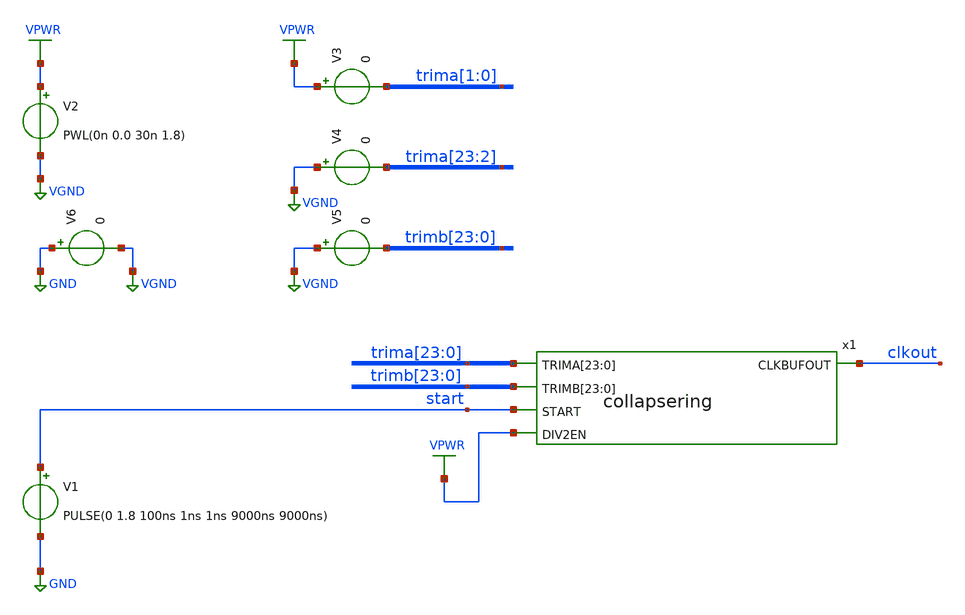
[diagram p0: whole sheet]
** sch_path: ip/randsack/sch/collapsering_tb.sch
**.subckt collapsering_tb
V1 start GND PULSE(0 1.8 100ns 1ns 1ns 9000ns 9000ns)
V2 VPWR VGND PWL(0n 0.0 30n 1.8)
x1 trima[23] trima[22] trima[21] trima[20] trima[19] trima[18] trima[17] trima[16] trima[15]
+ trima[14] trima[13] trima[12] trima[11] trima[10] trima[9] trima[8] trima[7] trima[6] trima[5] trima[4]
+ trima[3] trima[2] trima[1] trima[0] trimb[23] trimb[22] trimb[21] trimb[20] trimb[19] trimb[18] trimb[17]
+ trimb[16] trimb[15] trimb[14] trimb[13] trimb[12] trimb[11] trimb[10] trimb[9] trimb[8] trimb[7] trimb[6]
+ trimb[5] trimb[4] trimb[3] trimb[2] trimb[1] trimb[0] start clkout VPWR collapsering
V3 VPWR trima[1] 0
V4 VGND trima[23] 0
V5 VGND trimb[23] 0
V6 GND VGND 0
**** begin user architecture code


.lib /home/harrison/workspace/sky130/sky130A/libs.tech/ngspice/sky130.lib.spice tt
.include /home/harrison/workspace/sky130/sky130A/libs.ref/sky130_fd_sc_hd/spice/sky130_fd_sc_hd.spice

.control
save all
tran 0.1n 10u
set appendwrite
write collapsering_tb.out
.endc


**** end user architecture code
**.ends

* expanding   symbol:  /home/harrison/workspace/randsack/verilog/rtl/randsack/sch/collapsering.sym #
*+ of pins=5
** sym_path: ip/randsack/sch/collapsering.sym
** sch_path: ip/randsack/sch/collapsering.sch
.subckt collapsering TRIMA[23] TRIMA[22] TRIMA[21] TRIMA[20] TRIMA[19] TRIMA[18] TRIMA[17] TRIMA[16]
+ TRIMA[15] TRIMA[14] TRIMA[13] TRIMA[12] TRIMA[11] TRIMA[10] TRIMA[9] TRIMA[8] TRIMA[7] TRIMA[6] TRIMA[5]
+ TRIMA[4] TRIMA[3] TRIMA[2] TRIMA[1] TRIMA[0] TRIMB[23] TRIMB[22] TRIMB[21] TRIMB[20] TRIMB[19] TRIMB[18]
+ TRIMB[17] TRIMB[16] TRIMB[15] TRIMB[14] TRIMB[13] TRIMB[12] TRIMB[11] TRIMB[10] TRIMB[9] TRIMB[8] TRIMB[7]
+ TRIMB[6] TRIMB[5] TRIMB[4] TRIMB[3] TRIMB[2] TRIMB[1] TRIMB[0] START CLKBUFOUT DIV2EN
*.opin CLKBUFOUT
*.ipin START
*.ipin DIV2EN
*.ipin
*+ TRIMA[23],TRIMA[22],TRIMA[21],TRIMA[20],TRIMA[19],TRIMA[18],TRIMA[17],TRIMA[16],TRIMA[15],TRIMA[14],TRIMA[13],TRIMA[12],TRIMA[11],TRIMA[10],TRIMA[9],TRIMA[8],TRIMA[7],TRIMA[6],TRIMA[5],TRIMA[4],TRIMA[3],TRIMA[2],TRIMA[1],TRIMA[0]
*.ipin
*+ TRIMB[23],TRIMB[22],TRIMB[21],TRIMB[20],TRIMB[19],TRIMB[18],TRIMB[17],TRIMB[16],TRIMB[15],TRIMB[14],TRIMB[13],TRIMB[12],TRIMB[11],TRIMB[10],TRIMB[9],TRIMB[8],TRIMB[7],TRIMB[6],TRIMB[5],TRIMB[4],TRIMB[3],TRIMB[2],TRIMB[1],TRIMB[0]
x21 outb START VGND VNB VPB VPWR net1 sky130_fd_sc_hd__nand2_4
x47 START outa VGND VNB VPB VPWR net16 sky130_fd_sc_hd__nand2_4
x1 net2 net1 TRIMA[0] TRIMA[1] triminv
x2 net3 net2 TRIMA[2] TRIMA[3] triminv
x3 net4 net3 TRIMA[4] TRIMA[5] triminv
x4 net5 net4 TRIMA[6] TRIMA[7] triminv
x5 net6 net5 TRIMA[8] TRIMA[9] triminv
x6 net7 net6 TRIMA[10] TRIMA[11] triminv
x7 net8 net7 TRIMA[12] TRIMA[13] triminv
x8 net24 net8 TRIMA[14] TRIMA[15] triminv
x9 net9 net16 TRIMB[0] TRIMB[1] triminv
x10 net10 net9 TRIMB[2] TRIMB[3] triminv
x11 net11 net10 TRIMB[4] TRIMB[5] triminv
x12 net12 net11 TRIMB[6] TRIMB[7] triminv
x13 net13 net12 TRIMB[8] TRIMB[9] triminv
x14 net14 net13 TRIMB[10] TRIMB[11] triminv
x15 net15 net14 TRIMB[12] TRIMB[13] triminv
x16 net23 net15 TRIMB[14] TRIMB[15] triminv
x17 net17 net24 TRIMA[16] TRIMA[17] triminv
x18 net18 net17 TRIMA[18] TRIMA[19] triminv
x19 net19 net18 TRIMA[20] TRIMA[21] triminv
x20 outa net19 TRIMA[22] TRIMA[23] triminv
x26 net20 net23 TRIMB[16] TRIMB[17] triminv
x27 net21 net20 TRIMB[18] TRIMB[19] triminv
x28 net22 net21 TRIMB[20] TRIMB[21] triminv
x29 outb net22 TRIMB[22] TRIMB[23] triminv
x34 outa div2 DIV2EN VGND VNB VPB VPWR clkmux sky130_fd_sc_hd__mux2_4
x36 outa net25 VGND VNB VPB VPWR div2 net25 sky130_fd_sc_hd__dfxbp_2
x35 clkmux VGND VNB VPB VPWR CLKBUFOUT sky130_fd_sc_hd__clkbuf_4
.ends


* expanding   symbol:  /home/harrison/workspace/randsack/verilog/rtl/randsack/sch/triminv.sym # of
*+ pins=4
** sym_path: ip/randsack/sch/triminv.sym
** sch_path: ip/randsack/sch/triminv.sch
.subckt triminv OUT IN TRIM0 TRIM1
*.ipin IN
*.ipin OUT
*.ipin TRIM0
*.ipin TRIM1
x1 IN VGND VNB VPB VPWR ts sky130_fd_sc_hd__clkbuf_2
x2 ts TRIM1 VGND VNB VPB VPWR d1 sky130_fd_sc_hd__einvn_4
x3 d1 VGND VNB VPB VPWR d2 sky130_fd_sc_hd__clkinv_1
x4 d2 TRIM0 VGND VNB VPB VPWR OUT sky130_fd_sc_hd__einvp_2
x5 ts VGND VNB VPB VPWR d0 sky130_fd_sc_hd__clkbuf_1
x6 d0 TRIM1 VGND VNB VPB VPWR d1 sky130_fd_sc_hd__einvp_2
x7 ts TRIM0 VGND VNB VPB VPWR OUT sky130_fd_sc_hd__einvn_8
.ends

.GLOBAL GND
.GLOBAL VPWR
.GLOBAL VGND
.end
